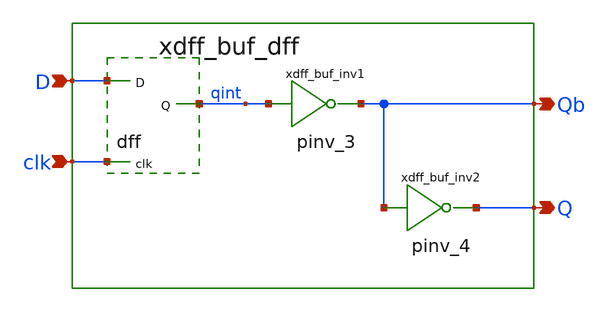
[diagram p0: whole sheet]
** sch_path: sram_2_64_scn4m/dff_buf_0.sch
**.subckt dff_buf_0 D Q Qb clk
*.ipin D
*.opin Q
*.opin Qb
*.ipin clk
xdff_buf_dff D qint clk vdd gnd dff
xdff_buf_inv1 qint Qb vdd gnd pinv_3
xdff_buf_inv2 Qb Q vdd gnd pinv_4
**.ends

* expanding   symbol:  dff.sym # of pins=3
** sym_path: sram_2_64_scn4m_lcc/dff.sym
** sch_path: sram_2_64_scn4m_lcc/dff.sch
.subckt dff D Q clk vdd gnd
*.ipin D
*.ipin clk
*.opin Q
M1013 net1 a_24_24# net2 gnd n w=5u l=0.18u m=1
M1012 net2 D gnd gnd n w=2u l=0.4u m=1
M1001 net3 D vdd vdd p w=4u l=0.4u m=1
M1002 net1 clk net3 vdd p w=4u l=0.4u m=1
M1000 a_24_24# clk vdd vdd p w=8u l=0.4u m=1
M1010 a_24_24# clk gnd gnd n w=4u l=0.4u m=1
M1005 a_152_16# net1 vdd vdd p w=4u l=0.4u m=1
M1016 a_152_16# net1 gnd gnd n w=5u l=0.4u m=1
M1004 net5 a_152_16# vdd vdd p w=4u l=0.4u m=1
M1003 net1 a_24_24# net5 vdd p w=4u l=0.4u m=1
M1014 net1 clk net4 gnd n w=2u l=0.4u m=1
M1015 net4 a_152_16# gnd gnd n w=2u l=0.4u m=1
M1006 net8 a_152_16# vdd vdd p w=4u l=0.4u m=1
M1007 net6 a_24_24# net8 vdd p w=4u l=0.4u m=1
M1018 net6 clk net7 gnd n w=2u l=0.4u m=1
M1017 net7 a_152_16# gnd gnd n w=2u l=0.4u m=1
M1021 Q net6 gnd gnd n w=4u l=0.4u m=1
M1011 Q net6 vdd vdd p w=8u l=0.4u m=1
M1020 net9 Q gnd gnd n w=2u l=0.4u m=1
M1019 net6 a_24_24# net9 gnd n w=2u l=0.4u m=1
M1009 net10 Q vdd vdd p w=2u l=0.4u m=1
M1008 net6 clk net10 vdd p w=2u l=0.4u m=1
.ends


* expanding   symbol:  pinv_3.sym # of pins=2
** sym_path: sram_2_64_scn4m_lcc/pinv_3.sym
** sch_path: sram_2_64_scn4m_lcc/pinv_3.sch
.subckt pinv_3 A Z vdd gnd
*.ipin A
*.opin Z
Mpinv_nmos Z A gnd gnd n w=1.6u l=0.4u m=1
Mp_inv_pmos Z A vdd vdd p w=3.2u l=0.4u m=1
.ends


* expanding   symbol:  pinv_4.sym # of pins=2
** sym_path: sram_2_64_scn4m/pinv_4.sym
** sch_path: sram_2_64_scn4m/pinv_4.sch
.subckt pinv_4 A Z vdd gnd
*.ipin A
*.opin Z
XMpinv_nmos Z A gnd gnd sky130_fd_pr__nfet_01v8 L=0.4 W=3.2 nf=1 ad='int((nf+1)/2) * W/nf * 0.29' as='int((nf+2)/2) * W/nf * 0.29'
+ pd='2*int((nf+1)/2) * (W/nf + 0.29)' ps='2*int((nf+2)/2) * (W/nf + 0.29)' nrd='0.29 / W' nrs='0.29 / W'
+ sa=0 sb=0 sd=0 mult=1 m=1
XMp_inv_pmos Z A vdd vdd sky130_fd_pr__pfet_01v8 L=0.4 W=6.4 nf=1 ad='int((nf+1)/2) * W/nf * 0.29' as='int((nf+2)/2) * W/nf * 0.29'
+ pd='2*int((nf+1)/2) * (W/nf + 0.29)' ps='2*int((nf+2)/2) * (W/nf + 0.29)' nrd='0.29 / W' nrs='0.29 / W'
+ sa=0 sb=0 sd=0 mult=1 m=1
.ends

.end
